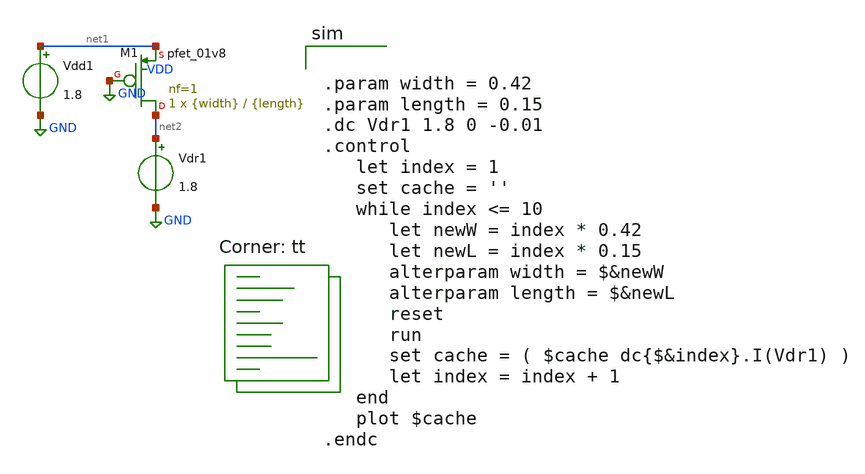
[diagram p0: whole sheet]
** sch_path: tutorial_2/tutorial_2_2c.sch
**.subckt tutorial_2_2c
Vdd1 net1 GND 1.8
XM1 net2 GND net1 VDD sky130_fd_pr__pfet_01v8 L={length} W={width} nf=1 ad='int((nf+1)/2) * W/nf * 0.29'
+ as='int((nf+2)/2) * W/nf * 0.29' pd='2*int((nf+1)/2) * (W/nf + 0.29)' ps='2*int((nf+2)/2) * (W/nf + 0.29)'
+ nrd='0.29 / W' nrs='0.29 / W' sa=0 sb=0 sd=0 mult=1 m=1
Vdr1 net2 GND 1.8
**** begin user architecture code


.param width = 0.42
.param length = 0.15
.dc Vdr1 1.8 0 -0.01
.control
   let index = 1
   set cache = ''
   while index <= 10
      let newW = index * 0.42
      let newL = index * 0.15
      alterparam width = $&newW
      alterparam length = $&newL
      reset
      run
      set cache = ( $cache dc{$&index}.I(Vdr1) )
      let index = index + 1
   end
   plot $cache
.endc

.lib $::SKYWATER_MODELS/sky130.lib.spice tt
**** end user architecture code
**.ends
.GLOBAL GND
.end
